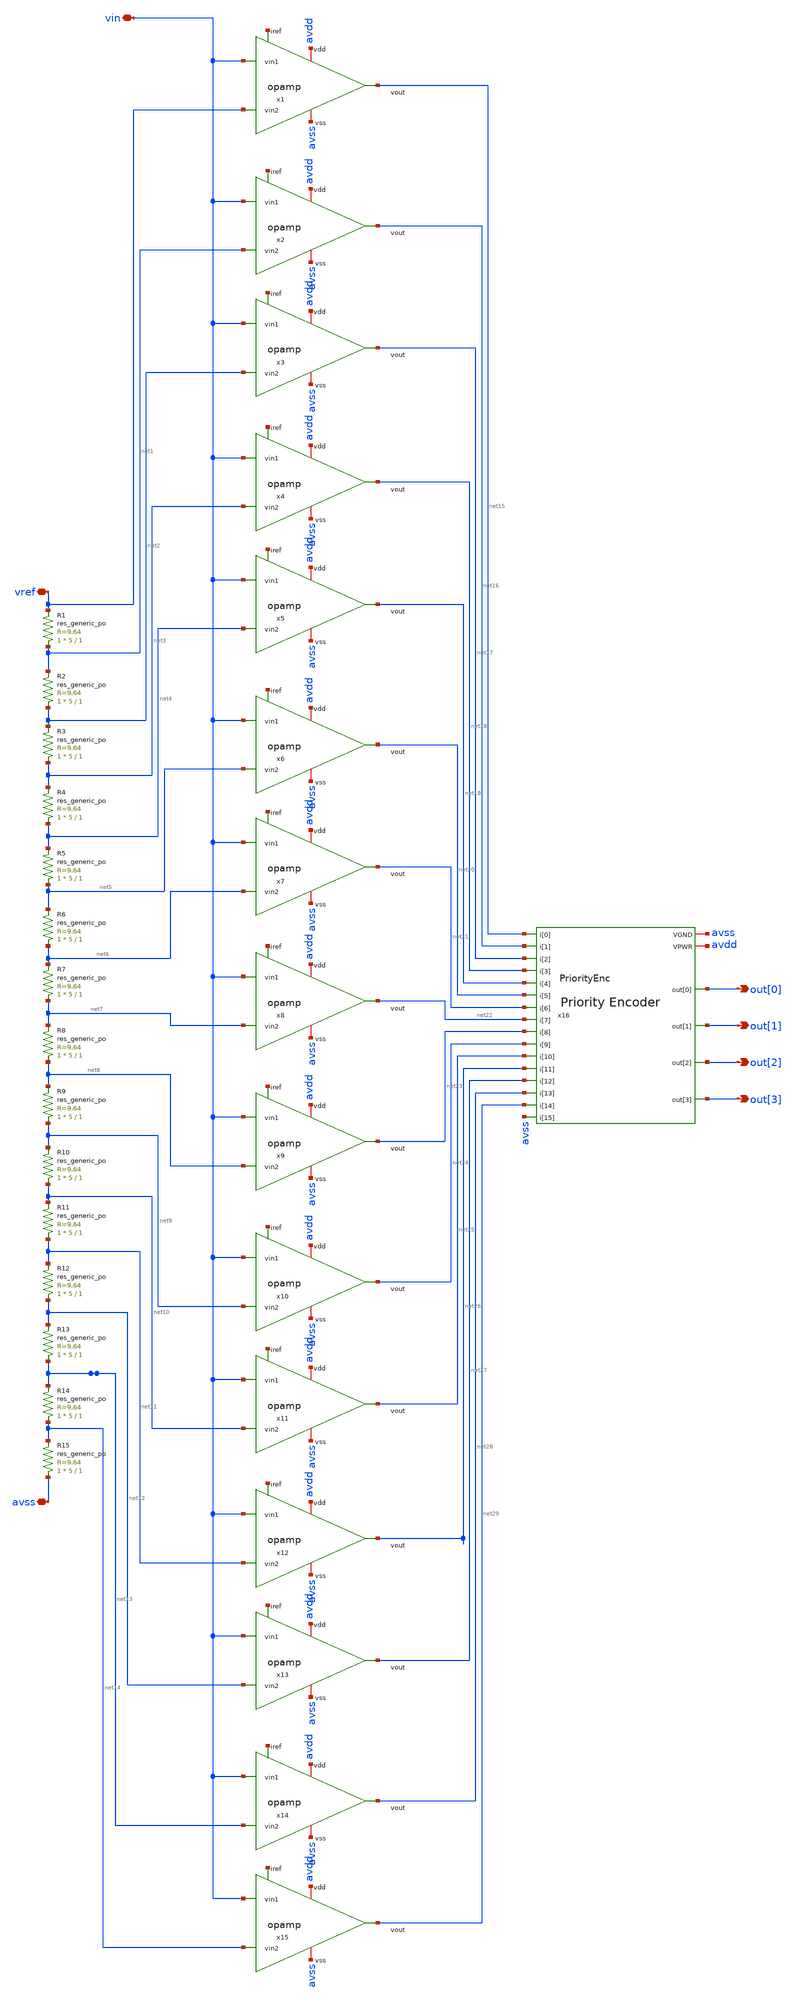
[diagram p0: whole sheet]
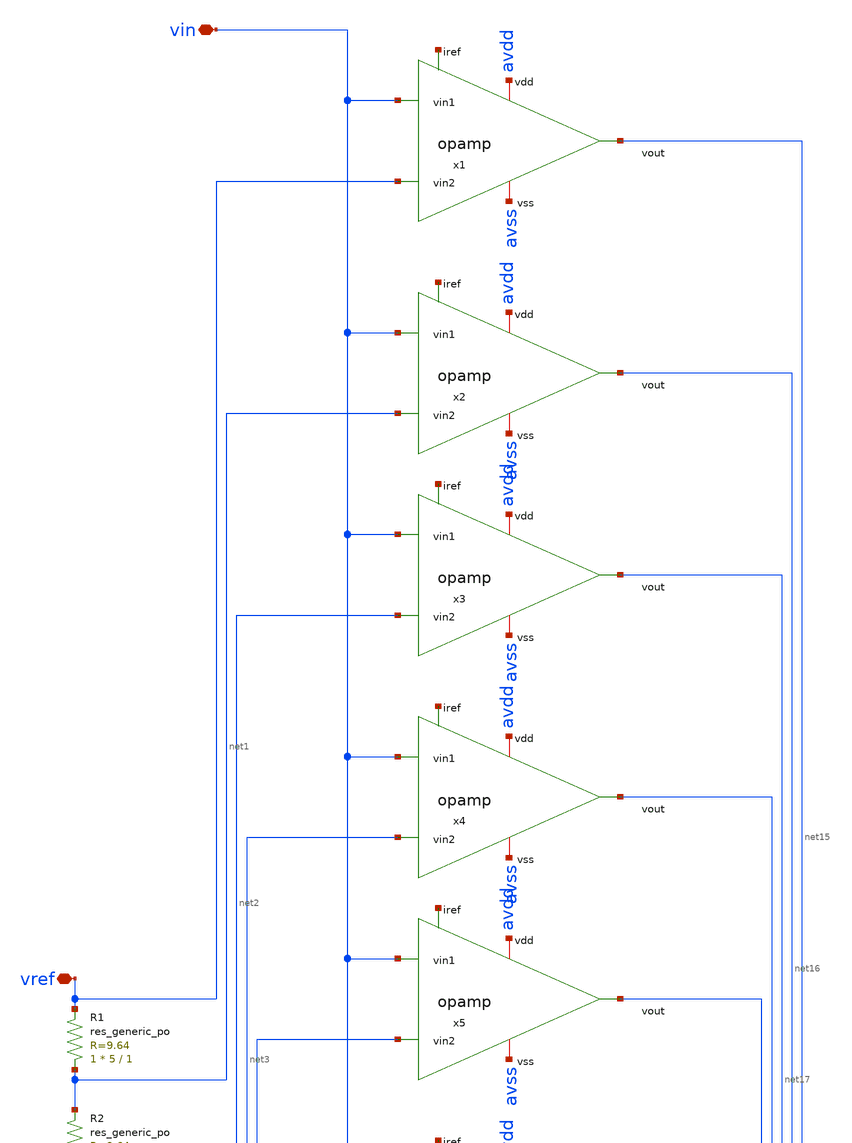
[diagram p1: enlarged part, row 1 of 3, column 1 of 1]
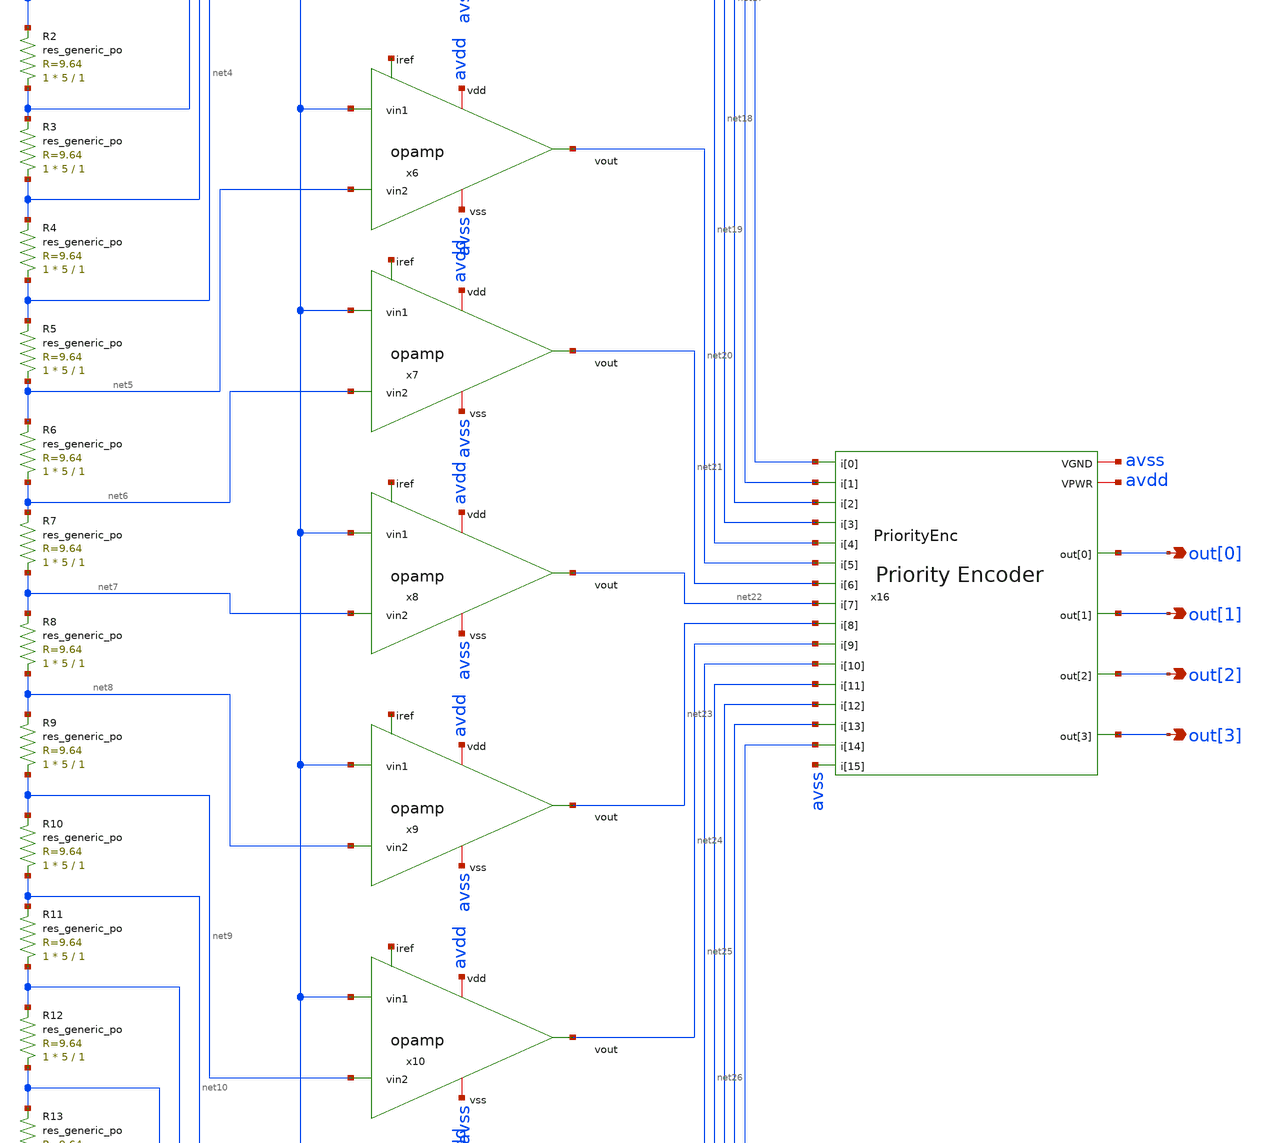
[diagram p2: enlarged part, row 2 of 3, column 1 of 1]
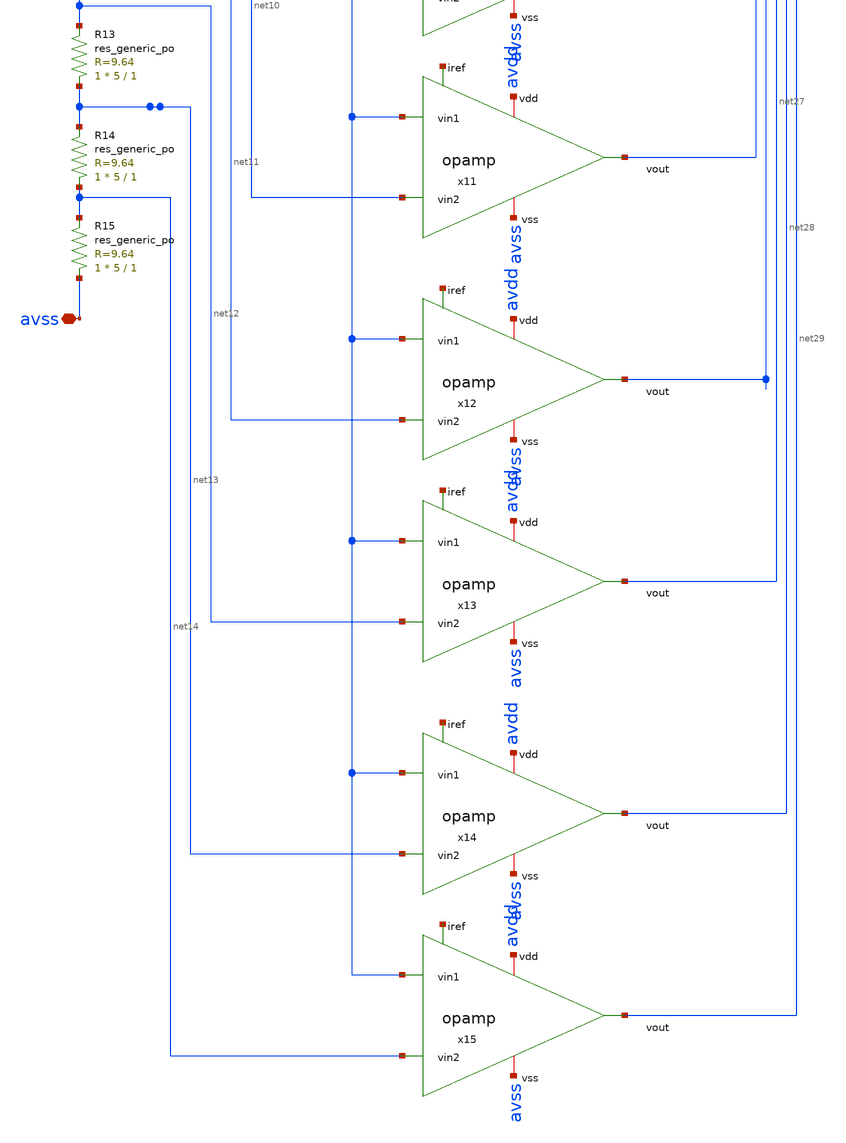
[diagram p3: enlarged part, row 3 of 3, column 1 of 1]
** sch_path: designs/libs/crossmem_ipn/adc4bits/adc4bits.sch
**.subckt adc4bits vref avss vin out[0] out[1] out[2] out[3]
*.iopin vref
*.iopin avss
*.iopin vin
*.opin out[0]
*.opin out[1]
*.opin out[2]
*.opin out[3]
XR1 net1 vref sky130_fd_pr__res_generic_po W=5 L=1 m=1
XR2 net2 net1 sky130_fd_pr__res_generic_po W=5 L=1 m=1
XR3 net3 net2 sky130_fd_pr__res_generic_po W=5 L=1 m=1
XR4 net4 net3 sky130_fd_pr__res_generic_po W=5 L=1 m=1
XR5 net5 net4 sky130_fd_pr__res_generic_po W=5 L=1 m=1
XR6 net6 net5 sky130_fd_pr__res_generic_po W=5 L=1 m=1
XR7 net7 net6 sky130_fd_pr__res_generic_po W=5 L=1 m=1
XR8 net8 net7 sky130_fd_pr__res_generic_po W=5 L=1 m=1
XR9 net9 net8 sky130_fd_pr__res_generic_po W=5 L=1 m=1
XR10 net10 net9 sky130_fd_pr__res_generic_po W=5 L=1 m=1
XR11 net11 net10 sky130_fd_pr__res_generic_po W=5 L=1 m=1
XR12 net12 net11 sky130_fd_pr__res_generic_po W=5 L=1 m=1
XR13 net13 net12 sky130_fd_pr__res_generic_po W=5 L=1 m=1
XR14 net14 net13 sky130_fd_pr__res_generic_po W=5 L=1 m=1
XR15 avss net14 sky130_fd_pr__res_generic_po W=5 L=1 m=1
x1 avdd vin vref net15 net30 avss opamp
x2 avdd vin net1 net16 net31 avss opamp
x3 avdd vin net2 net17 net32 avss opamp
x4 avdd vin net3 net18 net33 avss opamp
x5 avdd vin net4 net19 net34 avss opamp
x6 avdd vin net5 net20 net35 avss opamp
x7 avdd vin net6 net21 net36 avss opamp
x8 avdd vin net7 net22 net37 avss opamp
x9 avdd vin net8 net23 net38 avss opamp
x10 avdd vin net9 net24 net39 avss opamp
x11 avdd vin net10 net25 net40 avss opamp
x12 avdd vin net11 net26 net41 avss opamp
x13 avdd vin net12 net27 net42 avss opamp
x14 avdd vin net13 net28 net43 avss opamp
x15 avdd vin net14 net29 net44 avss opamp
x16 avss avdd net15 net25 net26 net27 net28 net29 avss net16 net17 net18 net19 net20 net21 net22
+ net23 net24 out[0] out[1] out[2] out[3] PriorityEnc
**** begin user architecture code


.inc /foss/designs/crossmem_ipn/designs/libs/crossmem_ipn/adc4bits/priorityEnc/runs/test/final/spice


**** end user architecture code
**.ends

* expanding   symbol:  /foss/designs/crossmem_ipn/designs/libs/crossmem_ipn/opamp/opamp.sym # of
*+ pins=6
** sym_path: designs/libs/crossmem_ipn/opamp/opamp.sym
** sch_path: designs/libs/crossmem_ipn/opamp/opamp.sch
.subckt opamp vdd vin1 vin2 vout iref vss
*.iopin vss
*.iopin vdd
*.opin vout
*.ipin iref
*.ipin vin1
*.ipin vin2
XM3 net1 net1 vdd vdd sky130_fd_pr__pfet_01v8 L=1 W=9 nf=1 ad='int((1 + 1)/2) * 9 / 1 * 0.29' as='int((1 + 2)/2) * 9 / 1 * 0.29'
+ pd='2*int((1 + 1)/2) * (9 / 1 + 0.29)' ps='2*int((1 + 2)/2) * (9 / 1 + 0.29)' nrd='0.29 / 9 ' nrs='0.29 / 9 '
+ sa=0 sb=0 sd=0 mult=1 m=1
XM4 net2 net1 vdd vdd sky130_fd_pr__pfet_01v8 L=1 W=9 nf=1 ad='int((1 + 1)/2) * 9 / 1 * 0.29' as='int((1 + 2)/2) * 9 / 1 * 0.29'
+ pd='2*int((1 + 1)/2) * (9 / 1 + 0.29)' ps='2*int((1 + 2)/2) * (9 / 1 + 0.29)' nrd='0.29 / 9 ' nrs='0.29 / 9 '
+ sa=0 sb=0 sd=0 mult=1 m=1
XM6 vout net2 vdd vdd sky130_fd_pr__pfet_01v8 L=1 W=8.65 nf=20 ad='int((20 + 1)/2) * 8.65 / 20 * 0.29'
+ as='int((20 + 2)/2) * 8.65 / 20 * 0.29' pd='2*int((20 + 1)/2) * (8.65 / 20 + 0.29)' ps='2*int((20 + 2)/2) * (8.65 / 20 + 0.29)'
+ nrd='0.29 / 8.65 ' nrs='0.29 / 8.65 ' sa=0 sb=0 sd=0 mult=1 m=1
XM1 net1 vin1 net3 vss sky130_fd_pr__nfet_01v8 L=1 W=5 nf=1 ad='int((1 + 1)/2) * 5 / 1 * 0.29' as='int((1 + 2)/2) * 5 / 1 * 0.29'
+ pd='2*int((1 + 1)/2) * (5 / 1 + 0.29)' ps='2*int((1 + 2)/2) * (5 / 1 + 0.29)' nrd='0.29 / 5 ' nrs='0.29 / 5 '
+ sa=0 sb=0 sd=0 mult=1 m=1
XM2 net2 vin2 net3 vss sky130_fd_pr__nfet_01v8 L=1 W=5 nf=1 ad='int((1 + 1)/2) * 5 / 1 * 0.29' as='int((1 + 2)/2) * 5 / 1 * 0.29'
+ pd='2*int((1 + 1)/2) * (5 / 1 + 0.29)' ps='2*int((1 + 2)/2) * (5 / 1 + 0.29)' nrd='0.29 / 5 ' nrs='0.29 / 5 '
+ sa=0 sb=0 sd=0 mult=1 m=1
XM5 net3 iref vss vss sky130_fd_pr__nfet_01v8 L=1 W=8 nf=1 ad='int((1 + 1)/2) * 8 / 1 * 0.29' as='int((1 + 2)/2) * 8 / 1 * 0.29'
+ pd='2*int((1 + 1)/2) * (8 / 1 + 0.29)' ps='2*int((1 + 2)/2) * (8 / 1 + 0.29)' nrd='0.29 / 8 ' nrs='0.29 / 8 '
+ sa=0 sb=0 sd=0 mult=1 m=1
XM8 iref iref vss vss sky130_fd_pr__nfet_01v8 L=1 W=8 nf=1 ad='int((1 + 1)/2) * 8 / 1 * 0.29' as='int((1 + 2)/2) * 8 / 1 * 0.29'
+ pd='2*int((1 + 1)/2) * (8 / 1 + 0.29)' ps='2*int((1 + 2)/2) * (8 / 1 + 0.29)' nrd='0.29 / 8 ' nrs='0.29 / 8 '
+ sa=0 sb=0 sd=0 mult=1 m=1
XM7 vout iref vss vss sky130_fd_pr__nfet_01v8 L=1 W=7 nf=16 ad='int((16 + 1)/2) * 7 / 16 * 0.29' as='int((16 + 2)/2) * 7 / 16 * 0.29'
+ pd='2*int((16 + 1)/2) * (7 / 16 + 0.29)' ps='2*int((16 + 2)/2) * (7 / 16 + 0.29)' nrd='0.29 / 7 ' nrs='0.29 / 7 '
+ sa=0 sb=0 sd=0 mult=1 m=1
XC1 net2 vout sky130_fd_pr__cap_mim_m3_1 W=38.73 L=38.73 MF=1 m=1
.ends

.end
